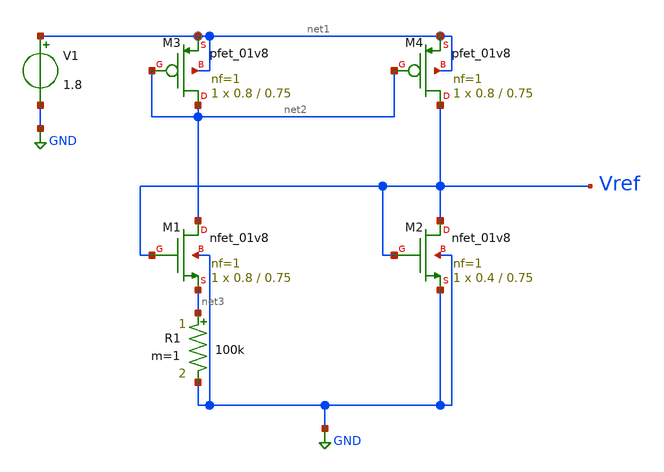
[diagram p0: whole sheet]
** sch_path: xschem/beta_mult_ref.sch
**.subckt beta_mult_ref
XM1 net2 Vref net3 GND sky130_fd_pr__nfet_01v8 L=0.75 W=0.8 nf=1 ad='int((nf+1)/2) * W/nf * 0.29' as='int((nf+2)/2) * W/nf * 0.29'
+ pd='2*int((nf+1)/2) * (W/nf + 0.29)' ps='2*int((nf+2)/2) * (W/nf + 0.29)' nrd='0.29 / W' nrs='0.29 / W'
+ sa=0 sb=0 sd=0 mult=1 m=1
XM2 Vref Vref GND GND sky130_fd_pr__nfet_01v8 L=0.75 W=0.4 nf=1 ad='int((nf+1)/2) * W/nf * 0.29' as='int((nf+2)/2) * W/nf * 0.29'
+ pd='2*int((nf+1)/2) * (W/nf + 0.29)' ps='2*int((nf+2)/2) * (W/nf + 0.29)' nrd='0.29 / W' nrs='0.29 / W'
+ sa=0 sb=0 sd=0 mult=1 m=1
XM3 net2 net2 net1 net1 sky130_fd_pr__pfet_01v8 L=0.75 W=0.8 nf=1 ad='int((nf+1)/2) * W/nf * 0.29' as='int((nf+2)/2) * W/nf * 0.29'
+ pd='2*int((nf+1)/2) * (W/nf + 0.29)' ps='2*int((nf+2)/2) * (W/nf + 0.29)' nrd='0.29 / W' nrs='0.29 / W'
+ sa=0 sb=0 sd=0 mult=1 m=1
XM4 Vref net2 net1 net1 sky130_fd_pr__pfet_01v8 L=0.75 W=0.8 nf=1 ad='int((nf+1)/2) * W/nf * 0.29' as='int((nf+2)/2) * W/nf * 0.29'
+ pd='2*int((nf+1)/2) * (W/nf + 0.29)' ps='2*int((nf+2)/2) * (W/nf + 0.29)' nrd='0.29 / W' nrs='0.29 / W'
+ sa=0 sb=0 sd=0 mult=1 m=1
V1 net1 GND 1.8
R1 net3 GND 100k m=1
**** begin user architecture code


.lib /usr/local/share/pdk/sky130A/libs.tech/ngspice/sky130.lib.spice tt
.save all
.control
        dc R1 1k 10000k 1k
        plot @m.xm2.msky130_fd_pr__nfet_01v8[id]
	plot v(Vref)
.endc


**** end user architecture code
**.ends
.GLOBAL GND
.end
